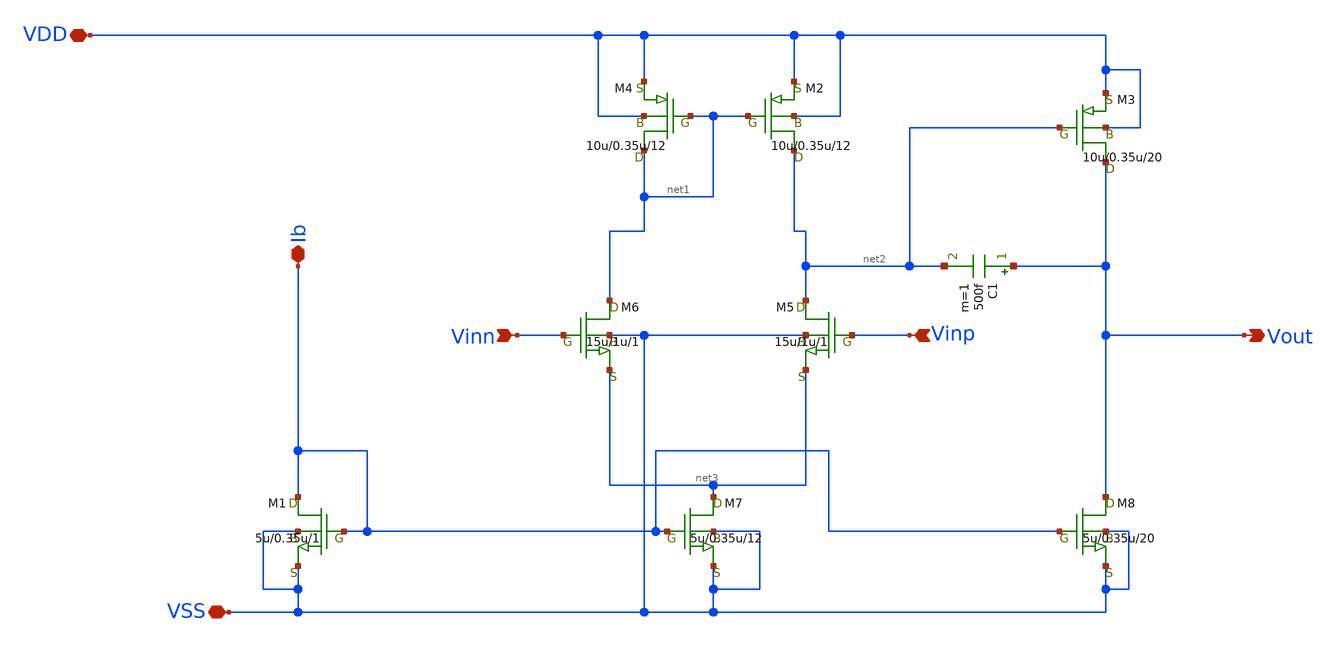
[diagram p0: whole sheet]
** sch_path: OPAmpN.sch
**.subckt OPAmpN Vout Vinn Vinp Ib VDD VSS
*.opin Vout
*.ipin Vinn
*.ipin Vinp
*.iopin Ib
*.iopin VDD
*.iopin VSS
M3 Vout net2 VDD VDD pch w=10u l=0.35u as=0 ps=0 ad=0 pd=0 m=20
M8 Vout Ib VSS VSS nch w=5u l=0.35u as=0 ps=0 ad=0 pd=0 m=20
C1 Vout net2 500f m=1
M5 net2 Vinp net3 VSS nch w=15u l=1u as=0 ps=0 ad=0 pd=0 m=1
M6 net1 Vinn net3 VSS nch w=15u l=1u as=0 ps=0 ad=0 pd=0 m=1
M2 net2 net1 VDD VDD pch w=10u l=0.35u as=0 ps=0 ad=0 pd=0 m=12
M4 net1 net1 VDD VDD pch w=10u l=0.35u as=0 ps=0 ad=0 pd=0 m=12
M7 net3 Ib VSS VSS nch w=5u l=0.35u as=0 ps=0 ad=0 pd=0 m=12
M1 Ib Ib VSS VSS nch w=5u l=0.35u as=0 ps=0 ad=0 pd=0 m=1
**.ends
.end
